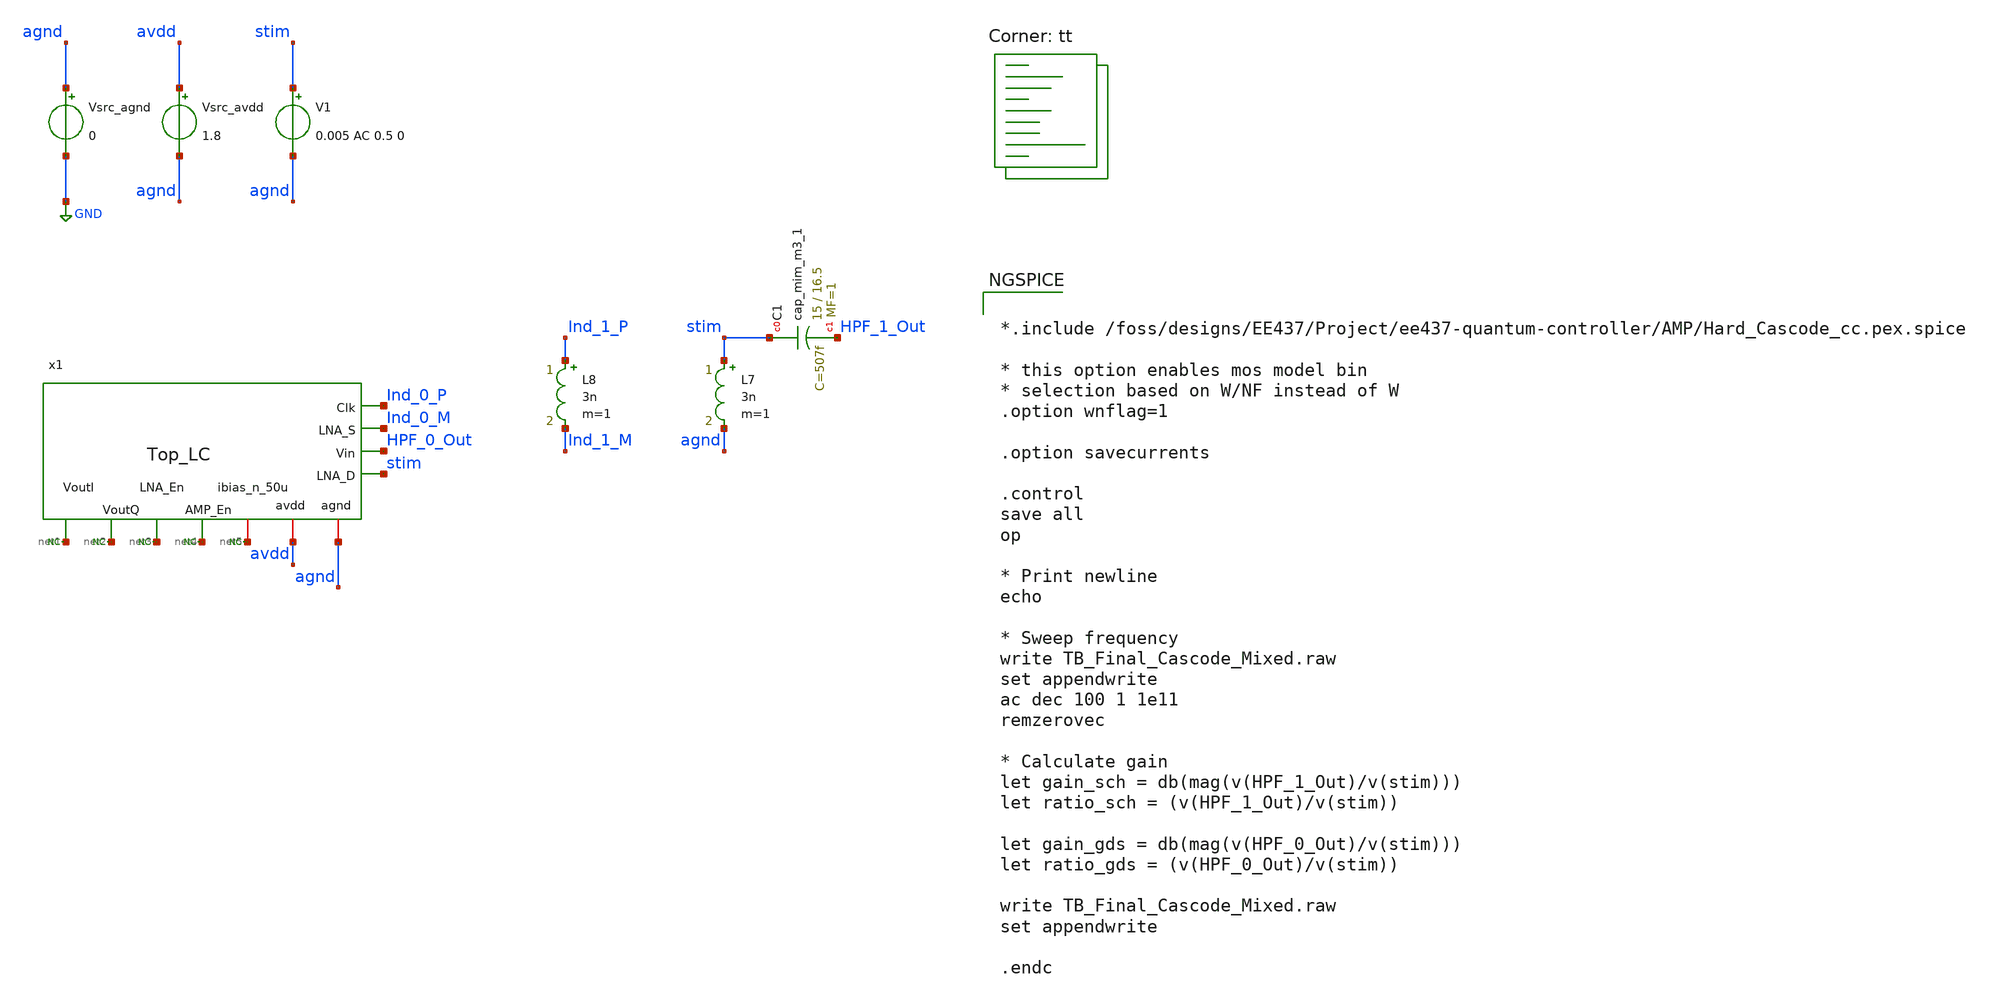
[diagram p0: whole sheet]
** sch_path: Top_Level/TB_Top_Level_LC.sch
**.subckt TB_Top_Level_LC
Vsrc_agnd agnd GND 0
Vsrc_avdd avdd agnd 1.8
* noconn #net5
* noconn #net4
* noconn #net3
* noconn #net2
* noconn #net1
XC1 stim HPF_1_Out sky130_fd_pr__cap_mim_m3_1 W=15 L=16.5 MF=1 m=1
V1 stim agnd 0.005 AC 0.5 0
L8 Ind_1_P Ind_1_M 3n m=1
L7 stim agnd 3n m=1
**** begin user architecture code


*.include /foss/designs/EE437/Project/ee437-quantum-controller/AMP/Hard_Cascode_cc.pex.spice

* this option enables mos model bin
* selection based on W/NF instead of W
.option wnflag=1

.option savecurrents

.control
save all
op

* Print newline
echo

* Sweep frequency
write TB_Final_Cascode_Mixed.raw
set appendwrite
ac dec 100 1 1e11
remzerovec

* Calculate gain
let gain_sch = db(mag(v(HPF_1_Out)/v(stim)))
let ratio_sch = (v(HPF_1_Out)/v(stim))

let gain_gds = db(mag(v(HPF_0_Out)/v(stim)))
let ratio_gds = (v(HPF_0_Out)/v(stim))

write TB_Final_Cascode_Mixed.raw
set appendwrite

.endc


.lib $::SKYWATER_MODELS/sky130.lib.spice tt
**** end user architecture code
**.ends
.GLOBAL GND
.end
